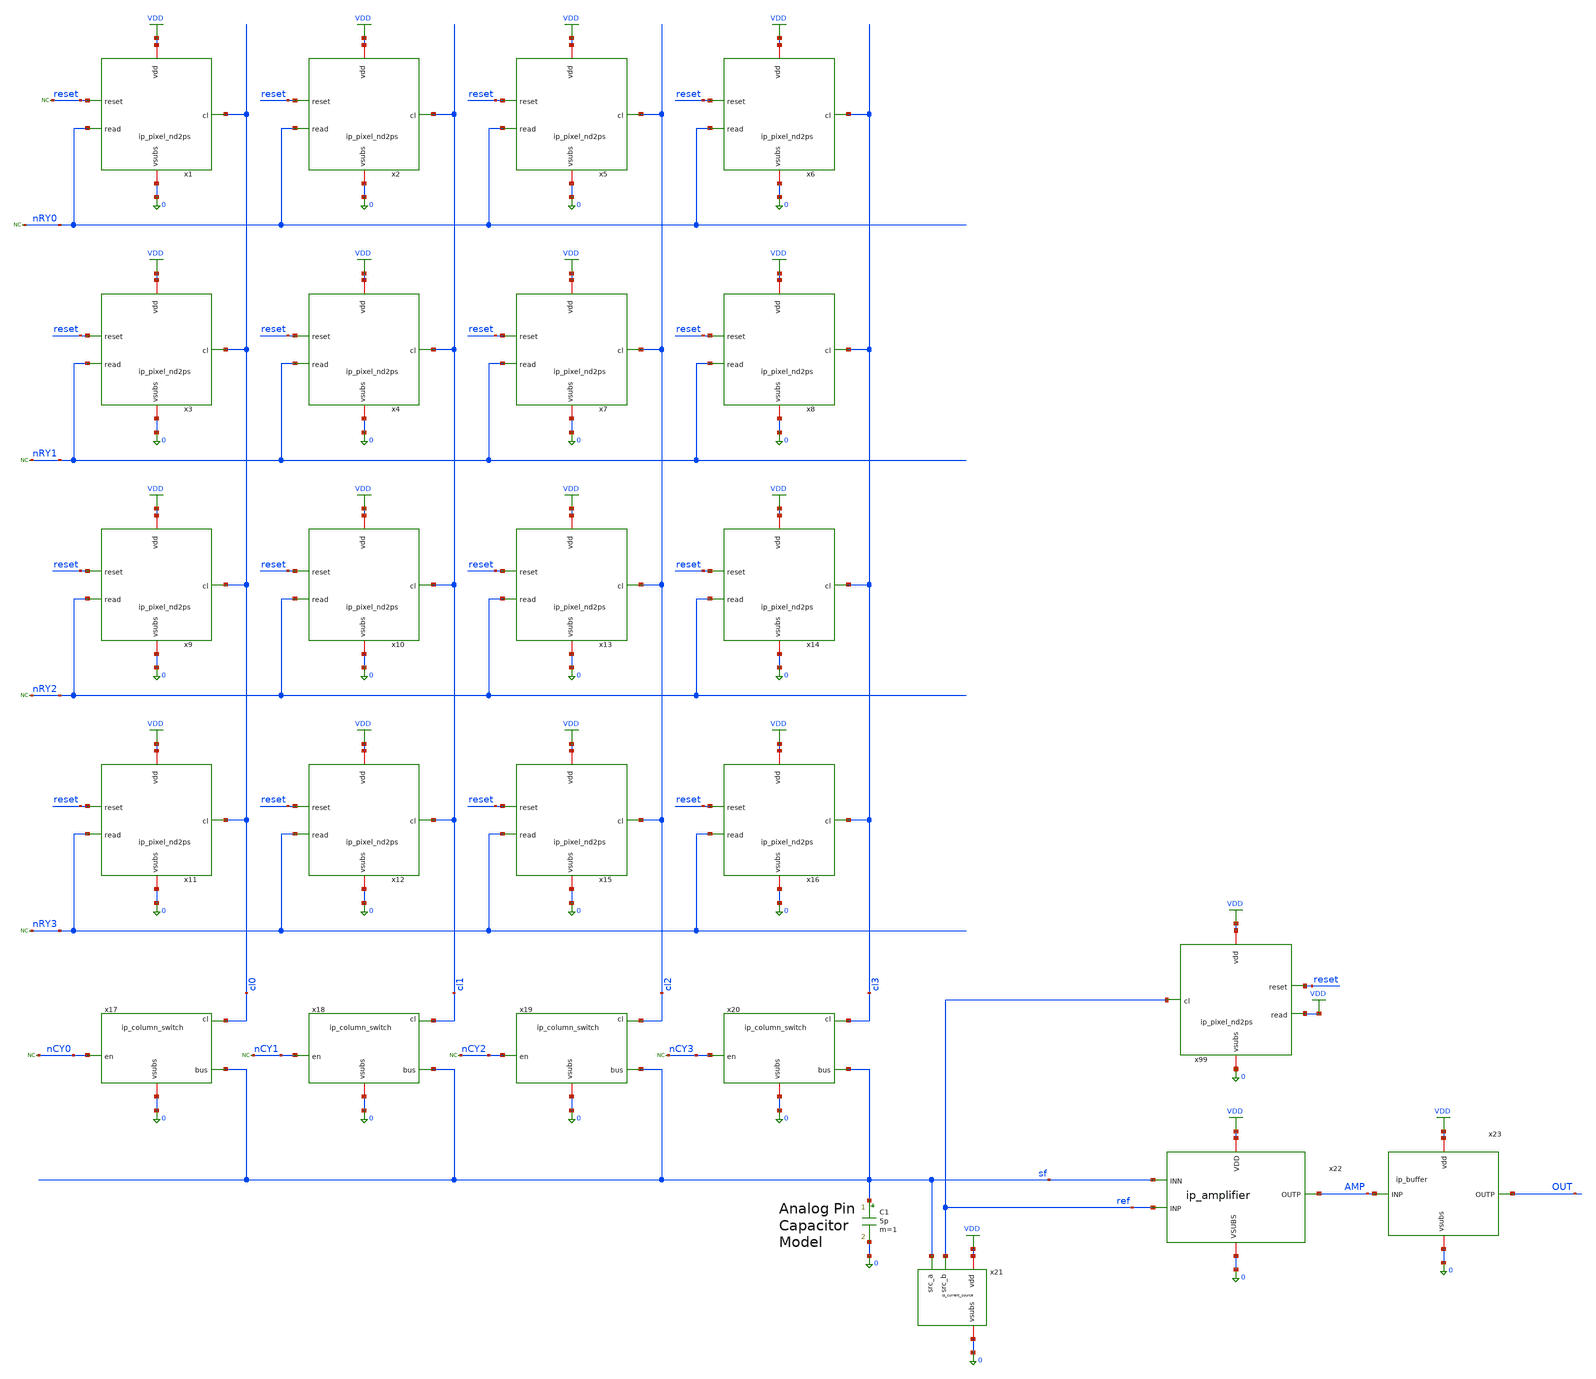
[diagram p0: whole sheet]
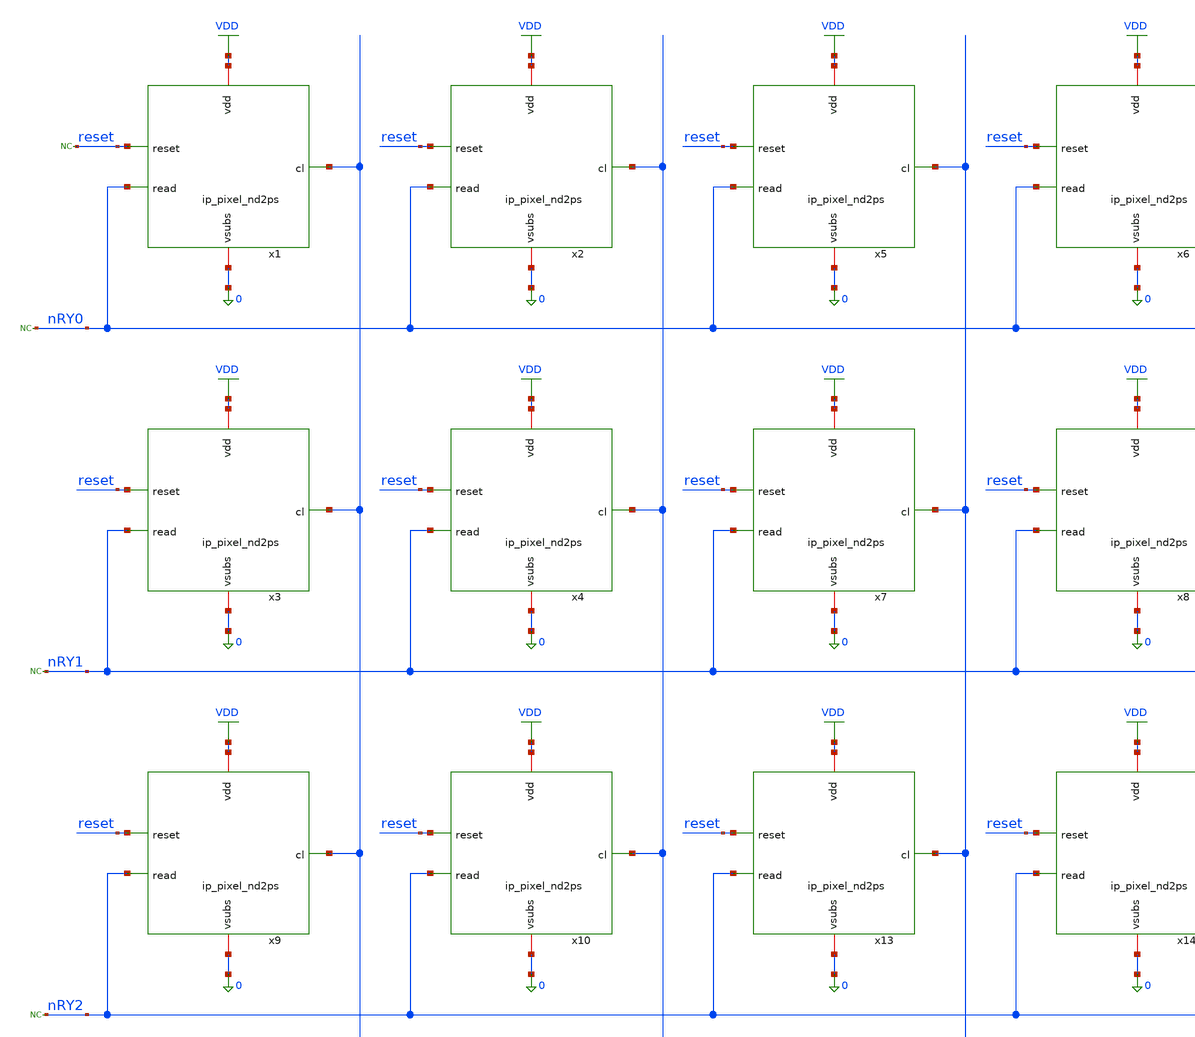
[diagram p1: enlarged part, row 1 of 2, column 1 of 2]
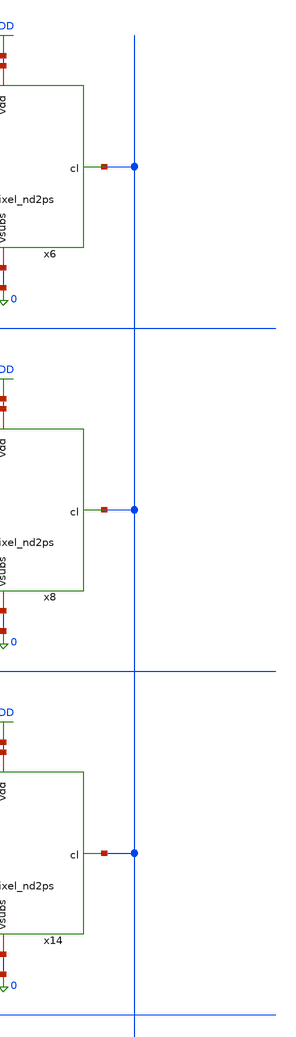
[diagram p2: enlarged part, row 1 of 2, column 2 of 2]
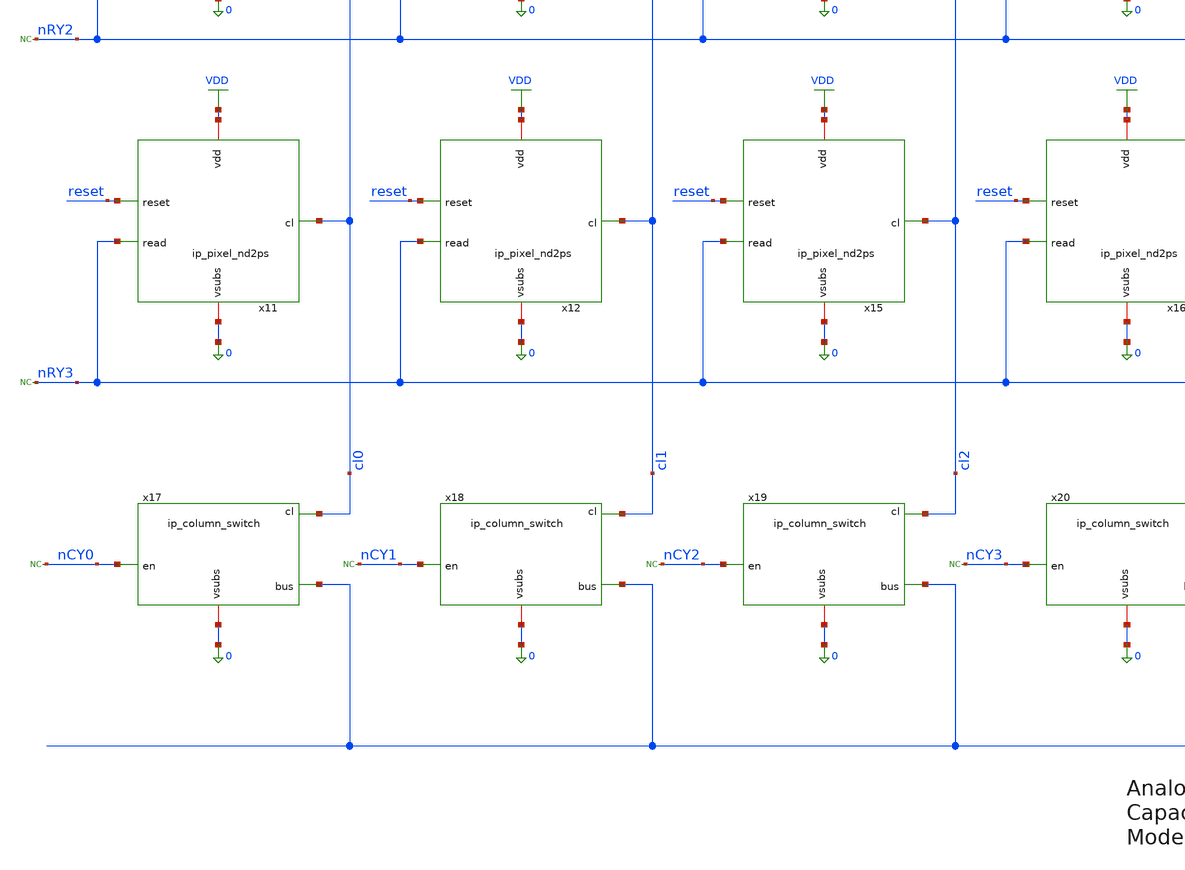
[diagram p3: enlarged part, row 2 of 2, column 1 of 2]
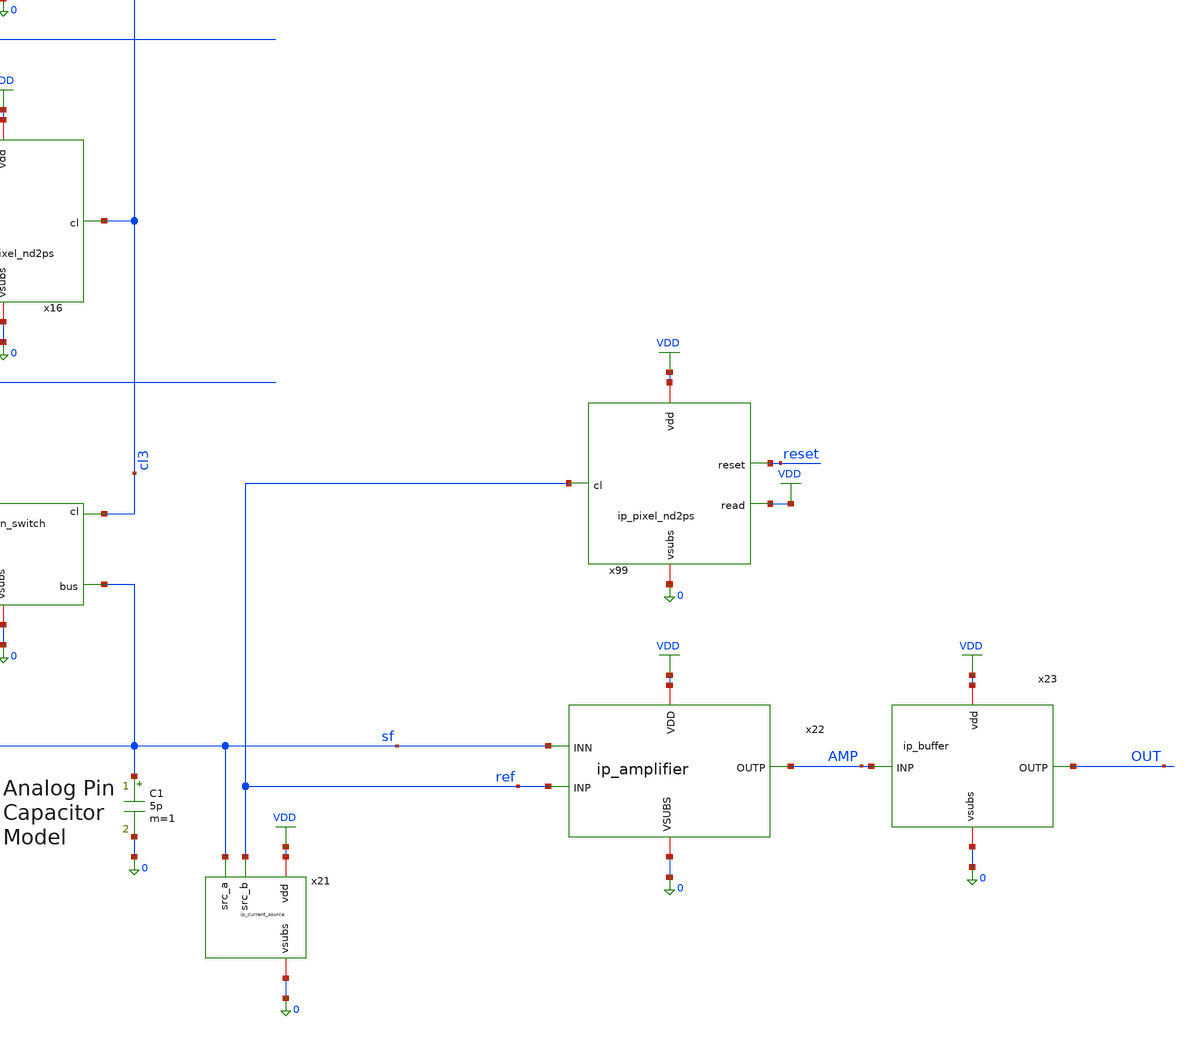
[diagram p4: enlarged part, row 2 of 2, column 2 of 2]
** sch_path: xschem/tb_total.sch
**.subckt tb_total
x1 VDD reset nRY0 0 cl0 ip_pixel_nd2ps
x2 VDD reset nRY0 0 cl1 ip_pixel_nd2ps
x3 VDD reset nRY1 0 cl0 ip_pixel_nd2ps
x4 VDD reset nRY1 0 cl1 ip_pixel_nd2ps
x5 VDD reset nRY0 0 cl2 ip_pixel_nd2ps
x6 VDD reset nRY0 0 cl3 ip_pixel_nd2ps
x7 VDD reset nRY1 0 cl2 ip_pixel_nd2ps
x8 VDD reset nRY1 0 cl3 ip_pixel_nd2ps
x9 VDD reset nRY2 0 cl0 ip_pixel_nd2ps
x10 VDD reset nRY2 0 cl1 ip_pixel_nd2ps
x11 VDD reset nRY3 0 cl0 ip_pixel_nd2ps
x12 VDD reset nRY3 0 cl1 ip_pixel_nd2ps
x13 VDD reset nRY2 0 cl2 ip_pixel_nd2ps
x14 VDD reset nRY2 0 cl3 ip_pixel_nd2ps
x15 VDD reset nRY3 0 cl2 ip_pixel_nd2ps
x16 VDD reset nRY3 0 cl3 ip_pixel_nd2ps
x17 cl0 sf nCY0 0 ip_column_switch
x18 cl1 sf nCY1 0 ip_column_switch
x19 cl2 sf nCY2 0 ip_column_switch
x20 cl3 sf nCY3 0 ip_column_switch
x21 VDD sf 0 ref ip_current_source
x22 VDD AMP ref sf 0 ip_amplifier
* noconn nRY0
* noconn nRY1
* noconn nRY2
* noconn nRY3
* noconn nCY0
* noconn nCY1
* noconn nCY2
* noconn nCY3
* noconn reset
x99 VDD reset VDD 0 ref ip_pixel_nd2ps
C1 sf 0 5p m=1
x23 VDD OUT AMP 0 ip_buffer
**** begin user architecture code

.include $::180MCU_MODELS/design.ngspice
.lib $::180MCU_MODELS/sm141064.ngspice typical
.lib $::180MCU_MODELS/sm141064.ngspice res_typical
.lib $::180MCU_MODELS/sm141064.ngspice moscap_typical
.lib $::180MCU_MODELS/sm141064.ngspice diode_typical




.control
	reset
	tran 1u 1.6m
	save all
	write tb_total.raw
	quit
.endc





VVDD VDD 0 3.3
VCLK CLK 0 PULSE (0 3.3 0 1n 1n 5u 10u)

astim [RESETA        nRA4 nRA3 nRA2 nRA1 nRA0        nCA4 nCA3 nCA2 nCA1 nCA0] stim
.model stim d_source input_file="../st_total.txt"

acosim[CLK        nCA4 nCA3 nCA2 nCA1 nCA0        nRA4 nRA3 nRA2 nRA1 nRA0        RESETA]
+        [reset        nCY20 nCY19 nCY18 nCY17 nCY16 nCY15        nCY14 nCY13 nCY12 nCY11 nCY10 nCY9         nCY8
+  nCY7  nCY6  nCY5  nCY4  nCY3         nCY2  nCY1  nCY0         nRY16 nRY15 nRY14 nRY13 nRY12 nRY11
+         nRY10 nRY9  nRY8  nRY7  nRY6  nRY5        nRY4  nRY3  nRY2  nRY1  nRY0        ] null dut
.model dut d_cosim simulation="../../verilog/rtl/aux_total_digital/aux_total_digital.so"

RnRA0  nRA0 0 100k
RnRA1  nRA1 0 100k
RnRA2  nRA2 0 100k
RnRA3  nRA3 0 100k
RnRA4  nRA4 0 100k

RnCA0  nCA0 0 100k
RnCA1  nCA1 0 100k
RnCA2  nCA2 0 100k
RnCA3  nCA3 0 100k
RnCA4  nCA4 0 100k

RnRY3  nRY3 0 100k
RnRY2  nRY2 0 100k
RnRY1  nRY1 0 100k
RnRY0  nRY0 0 100k

RnCY3  nCY3 0 100k
RnCY2  nCY2 0 100k
RnCY1  nCY1 0 100k
RnCY0  nCY0 0 100k

Rrsta  reseta 0 100k
Rrst   reset  0 100k

IPX1  x1.siminj  0 30p
IPX2  x2.siminj  0 22p
IPX3  x3.siminj  0 6p
IPX4  x4.siminj  0 28p
IPX5  x5.siminj  0 4p
IPX6  x6.siminj  0 20p
IPX7  x7.siminj  0 8p
IPX8  x8.siminj  0 12p
IPX9  x9.siminj  0 26p
IPX10 x10.siminj 0 14p
IPX11 x11.siminj 0 18p
IPX12 x12.siminj 0 10p
IPX13 x13.siminj 0 24p
IPX14 x14.siminj 0 0p
IPX15 x15.siminj 0 16p
IPX16 x16.siminj 0 2p


**** end user architecture code
**.ends

* expanding   symbol:  ip_pixel_nd2ps.sym # of pins=5
** sym_path: xschem/ip_pixel_nd2ps.sym
** sch_path: xschem/ip_pixel_nd2ps.sch
.subckt ip_pixel_nd2ps vdd reset read vsubs cl
*.iopin vdd
*.iopin vsubs
*.ipin reset
*.ipin read
*.opin cl
D2 vsubs siminj diode_nd2ps_06v0 area='13.5u * 13.5u ' pj='2*13.5u + 2*13.5u ' m=1
XM4 vdd siminj sfout vsubs nfet_06v0 L=1.0u W=2.5u nf=1 ad='int((nf+1)/2) * W/nf * 0.18u' as='int((nf+2)/2) * W/nf * 0.18u'
+ pd='2*int((nf+1)/2) * (W/nf + 0.18u)' ps='2*int((nf+2)/2) * (W/nf + 0.18u)' nrd='0.18u / W' nrs='0.18u / W'
+ sa=0 sb=0 sd=0 m=1 par=1
XM2 vdd reset siminj vsubs nfet_06v0 L=0.7u W=0.30u nf=1 ad='int((nf+1)/2) * W/nf * 0.18u' as='int((nf+2)/2) * W/nf * 0.18u'
+ pd='2*int((nf+1)/2) * (W/nf + 0.18u)' ps='2*int((nf+2)/2) * (W/nf + 0.18u)' nrd='0.18u / W' nrs='0.18u / W'
+ sa=0 sb=0 sd=0 m=1 par=1
XM1 sfout read cl vsubs nfet_06v0 L=0.7u W=0.30u nf=1 ad='int((nf+1)/2) * W/nf * 0.18u' as='int((nf+2)/2) * W/nf * 0.18u'
+ pd='2*int((nf+1)/2) * (W/nf + 0.18u)' ps='2*int((nf+2)/2) * (W/nf + 0.18u)' nrd='0.18u / W' nrs='0.18u / W'
+ sa=0 sb=0 sd=0 m=1 par=1
.ends


* expanding   symbol:  ip_column_switch.sym # of pins=4
** sym_path: xschem/ip_column_switch.sym
** sch_path: xschem/ip_column_switch.sch
.subckt ip_column_switch cl bus en vsubs
*.ipin cl
*.ipin en
*.iopin vsubs
*.opin bus
XM1 cl en bus vsubs nfet_06v0 L=0.7u W=0.5u nf=1 ad='int((nf+1)/2) * W/nf * 0.18u' as='int((nf+2)/2) * W/nf * 0.18u'
+ pd='2*int((nf+1)/2) * (W/nf + 0.18u)' ps='2*int((nf+2)/2) * (W/nf + 0.18u)' nrd='0.18u / W' nrs='0.18u / W'
+ sa=0 sb=0 sd=0 m=2 par=2
D1 vsubs en diode_nd2ps_06v0 area='0.5u * 0.5u ' pj='2*0.5u + 2*0.5u ' m=1
.ends


* expanding   symbol:  ip_current_source.sym # of pins=4
** sym_path: xschem/ip_current_source.sym
** sch_path: xschem/ip_current_source.sch
.subckt ip_current_source vdd src_a vsubs src_b
*.iopin vdd
*.iopin vsubs
*.ipin src_a
*.ipin src_b
XM8 refin refin vsubs vsubs nfet_06v0 L=1u W=5u nf=1 ad='int((nf+1)/2) * W/nf * 0.18u' as='int((nf+2)/2) * W/nf * 0.18u'
+ pd='2*int((nf+1)/2) * (W/nf + 0.18u)' ps='2*int((nf+2)/2) * (W/nf + 0.18u)' nrd='0.18u / W' nrs='0.18u / W'
+ sa=0 sb=0 sd=0 m=1 par=1
XM5 src_a refin net1 vsubs nfet_06v0 L=0.7u W=5u nf=1 ad='int((nf+1)/2) * W/nf * 0.18u' as='int((nf+2)/2) * W/nf * 0.18u'
+ pd='2*int((nf+1)/2) * (W/nf + 0.18u)' ps='2*int((nf+2)/2) * (W/nf + 0.18u)' nrd='0.18u / W' nrs='0.18u / W'
+ sa=0 sb=0 sd=0 m=2 par=2
XM3 src_b refin net2 vsubs nfet_06v0 L=0.7u W=5u nf=1 ad='int((nf+1)/2) * W/nf * 0.18u' as='int((nf+2)/2) * W/nf * 0.18u'
+ pd='2*int((nf+1)/2) * (W/nf + 0.18u)' ps='2*int((nf+2)/2) * (W/nf + 0.18u)' nrd='0.18u / W' nrs='0.18u / W'
+ sa=0 sb=0 sd=0 m=2 par=2
XM4 net1 refin vsubs vsubs nfet_06v0 L=5u W=0.5u nf=1 ad='int((nf+1)/2) * W/nf * 0.18u' as='int((nf+2)/2) * W/nf * 0.18u'
+ pd='2*int((nf+1)/2) * (W/nf + 0.18u)' ps='2*int((nf+2)/2) * (W/nf + 0.18u)' nrd='0.18u / W' nrs='0.18u / W'
+ sa=0 sb=0 sd=0 m=1 par=1
XM7 net2 refin vsubs vsubs nfet_06v0 L=5u W=0.5u nf=1 ad='int((nf+1)/2) * W/nf * 0.18u' as='int((nf+2)/2) * W/nf * 0.18u'
+ pd='2*int((nf+1)/2) * (W/nf + 0.18u)' ps='2*int((nf+2)/2) * (W/nf + 0.18u)' nrd='0.18u / W' nrs='0.18u / W'
+ sa=0 sb=0 sd=0 m=1 par=1
XR5 refin vdd vsubs ppolyf_u_1k_6p0 r_width=1e-6 r_length=42e-6 m=1
.ends


* expanding   symbol:  ip_amplifier.sym # of pins=5
** sym_path: xschem/ip_amplifier.sym
** sch_path: xschem/ip_amplifier.sch
.subckt ip_amplifier VDD OUTP INP INN VSUBS
*.iopin VDD
*.iopin VSUBS
*.ipin INP
*.ipin INN
*.opin OUTP
XM1 net10 INP net8 VDD pfet_06v0 L=0.7u W=11.0u nf=1 ad='int((nf+1)/2) * W/nf * 0.18u' as='int((nf+2)/2) * W/nf * 0.18u'
+ pd='2*int((nf+1)/2) * (W/nf + 0.18u)' ps='2*int((nf+2)/2) * (W/nf + 0.18u)' nrd='0.18u / W' nrs='0.18u / W'
+ sa=0 sb=0 sd=0 m=2 par=2
XM2 net9 INN net8 VDD pfet_06v0 L=0.7u W=11.0u nf=1 ad='int((nf+1)/2) * W/nf * 0.18u' as='int((nf+2)/2) * W/nf * 0.18u'
+ pd='2*int((nf+1)/2) * (W/nf + 0.18u)' ps='2*int((nf+2)/2) * (W/nf + 0.18u)' nrd='0.18u / W' nrs='0.18u / W'
+ sa=0 sb=0 sd=0 m=2 par=2
XM5 net10 net1 VSUBS vsubs nfet_06v0 L=2u W=5u nf=1 ad='int((nf+1)/2) * W/nf * 0.18u' as='int((nf+2)/2) * W/nf * 0.18u'
+ pd='2*int((nf+1)/2) * (W/nf + 0.18u)' ps='2*int((nf+2)/2) * (W/nf + 0.18u)' nrd='0.18u / W' nrs='0.18u / W'
+ sa=0 sb=0 sd=0 m=1 par=1
XM6 net9 net1 VSUBS vsubs nfet_06v0 L=2u W=5u nf=1 ad='int((nf+1)/2) * W/nf * 0.18u' as='int((nf+2)/2) * W/nf * 0.18u'
+ pd='2*int((nf+1)/2) * (W/nf + 0.18u)' ps='2*int((nf+2)/2) * (W/nf + 0.18u)' nrd='0.18u / W' nrs='0.18u / W'
+ sa=0 sb=0 sd=0 m=1 par=1
XM3 net3 net1 VSUBS vsubs nfet_06v0 L=1u W=12.5u nf=1 ad='int((nf+1)/2) * W/nf * 0.18u' as='int((nf+2)/2) * W/nf * 0.18u'
+ pd='2*int((nf+1)/2) * (W/nf + 0.18u)' ps='2*int((nf+2)/2) * (W/nf + 0.18u)' nrd='0.18u / W' nrs='0.18u / W'
+ sa=0 sb=0 sd=0 m=2 par=2
XM4 net2 net1 VSUBS vsubs nfet_06v0 L=1u W=5u nf=1 ad='int((nf+1)/2) * W/nf * 0.18u' as='int((nf+2)/2) * W/nf * 0.18u'
+ pd='2*int((nf+1)/2) * (W/nf + 0.18u)' ps='2*int((nf+2)/2) * (W/nf + 0.18u)' nrd='0.18u / W' nrs='0.18u / W'
+ sa=0 sb=0 sd=0 m=1 par=1
XM7 net1 net1 net3 vsubs nfet_06v0 L=0.7u W=14u nf=1 ad='int((nf+1)/2) * W/nf * 0.18u' as='int((nf+2)/2) * W/nf * 0.18u'
+ pd='2*int((nf+1)/2) * (W/nf + 0.18u)' ps='2*int((nf+2)/2) * (W/nf + 0.18u)' nrd='0.18u / W' nrs='0.18u / W'
+ sa=0 sb=0 sd=0 m=2 par=2
XM8 net4 net1 net2 vsubs nfet_06v0 L=0.7u W=14u nf=1 ad='int((nf+1)/2) * W/nf * 0.18u' as='int((nf+2)/2) * W/nf * 0.18u'
+ pd='2*int((nf+1)/2) * (W/nf + 0.18u)' ps='2*int((nf+2)/2) * (W/nf + 0.18u)' nrd='0.18u / W' nrs='0.18u / W'
+ sa=0 sb=0 sd=0 m=2 par=2
XM9 net5 net7 VDD VDD pfet_06v0 L=1u W=6u nf=1 ad='int((nf+1)/2) * W/nf * 0.18u' as='int((nf+2)/2) * W/nf * 0.18u'
+ pd='2*int((nf+1)/2) * (W/nf + 0.18u)' ps='2*int((nf+2)/2) * (W/nf + 0.18u)' nrd='0.18u / W' nrs='0.18u / W'
+ sa=0 sb=0 sd=0 m=1 par=1
XM10 net6 net7 VDD VDD pfet_06v0 L=1u W=6u nf=1 ad='int((nf+1)/2) * W/nf * 0.18u' as='int((nf+2)/2) * W/nf * 0.18u'
+ pd='2*int((nf+1)/2) * (W/nf + 0.18u)' ps='2*int((nf+2)/2) * (W/nf + 0.18u)' nrd='0.18u / W' nrs='0.18u / W'
+ sa=0 sb=0 sd=0 m=1 par=1
XM11 net7 net7 net5 VDD pfet_06v0 L=0.7u W=14u nf=1 ad='int((nf+1)/2) * W/nf * 0.18u' as='int((nf+2)/2) * W/nf * 0.18u'
+ pd='2*int((nf+1)/2) * (W/nf + 0.18u)' ps='2*int((nf+2)/2) * (W/nf + 0.18u)' nrd='0.18u / W' nrs='0.18u / W'
+ sa=0 sb=0 sd=0 m=2 par=2
XM12 net8 net7 net6 VDD pfet_06v0 L=0.7u W=14u nf=1 ad='int((nf+1)/2) * W/nf * 0.18u' as='int((nf+2)/2) * W/nf * 0.18u'
+ pd='2*int((nf+1)/2) * (W/nf + 0.18u)' ps='2*int((nf+2)/2) * (W/nf + 0.18u)' nrd='0.18u / W' nrs='0.18u / W'
+ sa=0 sb=0 sd=0 m=2 par=2
XM13 net11 net1 net9 vsubs nfet_06v0 L=0.7u W=12u nf=1 ad='int((nf+1)/2) * W/nf * 0.18u' as='int((nf+2)/2) * W/nf * 0.18u'
+ pd='2*int((nf+1)/2) * (W/nf + 0.18u)' ps='2*int((nf+2)/2) * (W/nf + 0.18u)' nrd='0.18u / W' nrs='0.18u / W'
+ sa=0 sb=0 sd=0 m=1 par=1
XM14 COMP net1 net10 vsubs nfet_06v0 L=0.7u W=12u nf=1 ad='int((nf+1)/2) * W/nf * 0.18u' as='int((nf+2)/2) * W/nf * 0.18u'
+ pd='2*int((nf+1)/2) * (W/nf + 0.18u)' ps='2*int((nf+2)/2) * (W/nf + 0.18u)' nrd='0.18u / W' nrs='0.18u / W'
+ sa=0 sb=0 sd=0 m=1 par=1
XM15 net11 net11 VDD VDD pfet_06v0 L=0.7u W=12u nf=1 ad='int((nf+1)/2) * W/nf * 0.18u' as='int((nf+2)/2) * W/nf * 0.18u'
+ pd='2*int((nf+1)/2) * (W/nf + 0.18u)' ps='2*int((nf+2)/2) * (W/nf + 0.18u)' nrd='0.18u / W' nrs='0.18u / W'
+ sa=0 sb=0 sd=0 m=1 par=1
XM16 COMP net11 VDD VDD pfet_06v0 L=0.7u W=12u nf=1 ad='int((nf+1)/2) * W/nf * 0.18u' as='int((nf+2)/2) * W/nf * 0.18u'
+ pd='2*int((nf+1)/2) * (W/nf + 0.18u)' ps='2*int((nf+2)/2) * (W/nf + 0.18u)' nrd='0.18u / W' nrs='0.18u / W'
+ sa=0 sb=0 sd=0 m=1 par=1
XM17 OUTP COMP VDD VDD pfet_06v0 L=0.7u W=12u nf=1 ad='int((nf+1)/2) * W/nf * 0.18u' as='int((nf+2)/2) * W/nf * 0.18u'
+ pd='2*int((nf+1)/2) * (W/nf + 0.18u)' ps='2*int((nf+2)/2) * (W/nf + 0.18u)' nrd='0.18u / W' nrs='0.18u / W'
+ sa=0 sb=0 sd=0 m=5 par=5
XM18 OUTP net10 VSUBS vsubs nfet_06v0 L=0.7u W=12u nf=1 ad='int((nf+1)/2) * W/nf * 0.18u' as='int((nf+2)/2) * W/nf * 0.18u'
+ pd='2*int((nf+1)/2) * (W/nf + 0.18u)' ps='2*int((nf+2)/2) * (W/nf + 0.18u)' nrd='0.18u / W' nrs='0.18u / W'
+ sa=0 sb=0 sd=0 m=3 par=3
XR3 net1 net14 vsubs ppolyf_u_1k_6p0 r_width=1e-6 r_length=6e-6 m=1
XR6 net14 net13 vsubs ppolyf_u_1k_6p0 r_width=1e-6 r_length=6e-6 m=1
XR7 net13 net12 vsubs ppolyf_u_1k_6p0 r_width=1e-6 r_length=6e-6 m=1
XR8 net12 net15 vsubs ppolyf_u_1k_6p0 r_width=1e-6 r_length=4e-6 m=1
Vmeas VDD net15 0
Vmeas1 net7 net4 0
XC1 OUTP net16 cap_nmos_03v3 c_width=12e-6 c_length=18e-6 m=1
XC2 COMP net17 cap_nmos_03v3 c_width=12e-6 c_length=18e-6 m=1
XR12 net16 COMP vsubs ppolyf_u_1k_6p0 r_width=1e-6 r_length=10e-6 m=1
XR16 OUTP net17 vsubs ppolyf_u_1k_6p0 r_width=1e-6 r_length=10e-6 m=1
.ends


* expanding   symbol:  ip_buffer.sym # of pins=4
** sym_path: xschem/ip_buffer.sym
** sch_path: xschem/ip_buffer.sch
.subckt ip_buffer vdd OUTP INP vsubs
*.iopin vsubs
*.iopin vdd
*.ipin INP
*.opin OUTP
XM1 vsubs INP OUTP OUTP pfet_06v0 L=1u W=10u nf=1 ad='int((nf+1)/2) * W/nf * 0.18u' as='int((nf+2)/2) * W/nf * 0.18u'
+ pd='2*int((nf+1)/2) * (W/nf + 0.18u)' ps='2*int((nf+2)/2) * (W/nf + 0.18u)' nrd='0.18u / W' nrs='0.18u / W'
+ sa=0 sb=0 sd=0 m=15
Vmeas net1 net2 0
XM4 OUTP net1 vdd vdd pfet_06v0 L=2u W=10u nf=1 ad='int((nf+1)/2) * W/nf * 0.18u' as='int((nf+2)/2) * W/nf * 0.18u'
+ pd='2*int((nf+1)/2) * (W/nf + 0.18u)' ps='2*int((nf+2)/2) * (W/nf + 0.18u)' nrd='0.18u / W' nrs='0.18u / W'
+ sa=0 sb=0 sd=0 m=5
XM2 net1 net1 vdd vdd pfet_06v0 L=2u W=10u nf=1 ad='int((nf+1)/2) * W/nf * 0.18u' as='int((nf+2)/2) * W/nf * 0.18u'
+ pd='2*int((nf+1)/2) * (W/nf + 0.18u)' ps='2*int((nf+2)/2) * (W/nf + 0.18u)' nrd='0.18u / W' nrs='0.18u / W'
+ sa=0 sb=0 sd=0 m=4
XR1 net4 net2 vsubs ppolyf_u_1k_6p0 r_width=1e-6 r_length=6e-6 m=1
XR2 net3 net4 vsubs ppolyf_u_1k_6p0 r_width=1e-6 r_length=6e-6 m=1
XR3 net5 net3 vsubs ppolyf_u_1k_6p0 r_width=1e-6 r_length=6e-6 m=1
XR4 vsubs net5 vsubs ppolyf_u_1k_6p0 r_width=1e-6 r_length=6e-6 m=1
.ends

.GLOBAL VDD
.end
